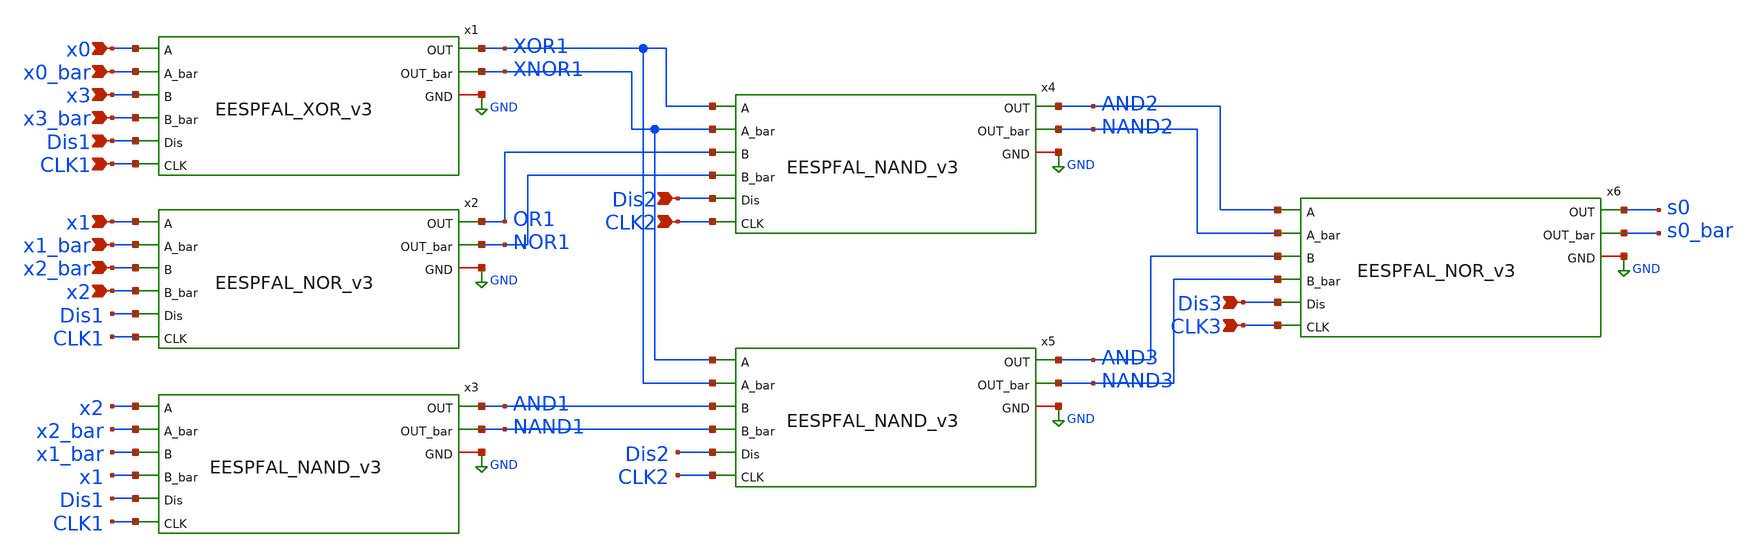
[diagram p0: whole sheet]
** sch_path: skywater_stuff/untitled-1.sch
**.subckt untitled-1 x0 x0_bar x3 x3_bar Dis1 CLK1 x1 x1_bar x2_bar x2 Dis2 CLK2 Dis3 CLK3
*.ipin x0
*.ipin x0_bar
*.ipin x3
*.ipin x3_bar
*.ipin Dis1
*.ipin CLK1
*.ipin x1
*.ipin x1_bar
*.ipin x2_bar
*.ipin x2
*.ipin Dis2
*.ipin CLK2
*.ipin Dis3
*.ipin CLK3
x2 x1 x1_bar x2_bar x2 OR1 NOR1 Dis1 GND CLK1 EESPFAL_NOR_v3
x3 x2 x2_bar x1_bar x1 AND1 NAND1 Dis1 GND CLK1 EESPFAL_NAND_v3
x1 x0 x0_bar x3 x3_bar XOR1 XNOR1 Dis1 GND CLK1 EESPFAL_XOR_v3
x4 XOR1 XNOR1 OR1 NOR1 AND2 NAND2 Dis2 GND CLK2 EESPFAL_NAND_v3
x5 XNOR1 XOR1 AND1 NAND1 AND3 NAND3 Dis2 GND CLK2 EESPFAL_NAND_v3
x6 AND2 NAND2 AND3 NAND3 s0 s0_bar Dis3 GND CLK3 EESPFAL_NOR_v3
**.ends
.GLOBAL GND
.end
